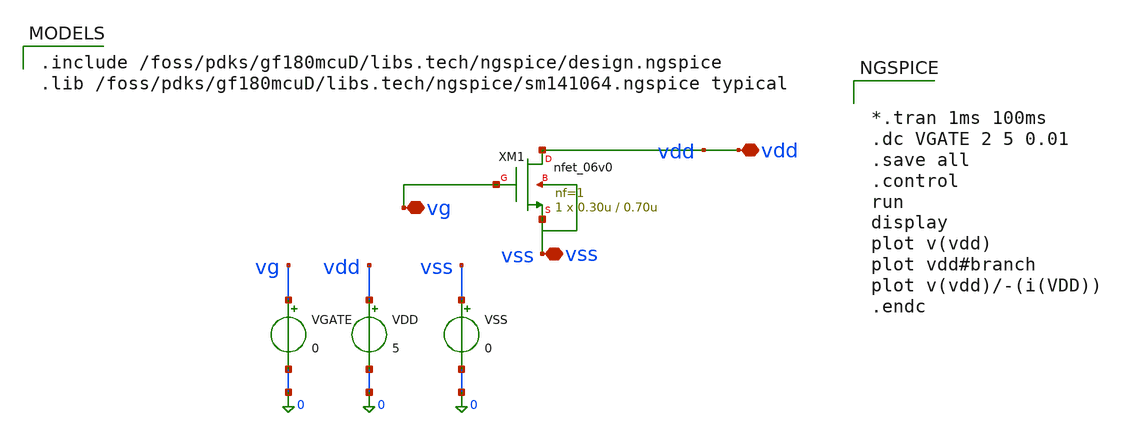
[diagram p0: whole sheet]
** sch_path: activities/opamp3An/NMOSresistor_tb.sch
**.subckt NMOSresistor_tb
VGATE vg 0 0
VDD vdd 0 5
VSS vss 0 0
**** begin user architecture code

.include /foss/pdks/gf180mcuD/libs.tech/ngspice/design.ngspice
.lib /foss/pdks/gf180mcuD/libs.tech/ngspice/sm141064.ngspice typical



*.tran 1ms 100ms
.dc VGATE 2 5 0.01
.save all
.control
run
display
plot v(vdd)
plot vdd#branch
plot v(vdd)/-(i(VDD))
.endc


**** end user architecture code
**.ends
.end
